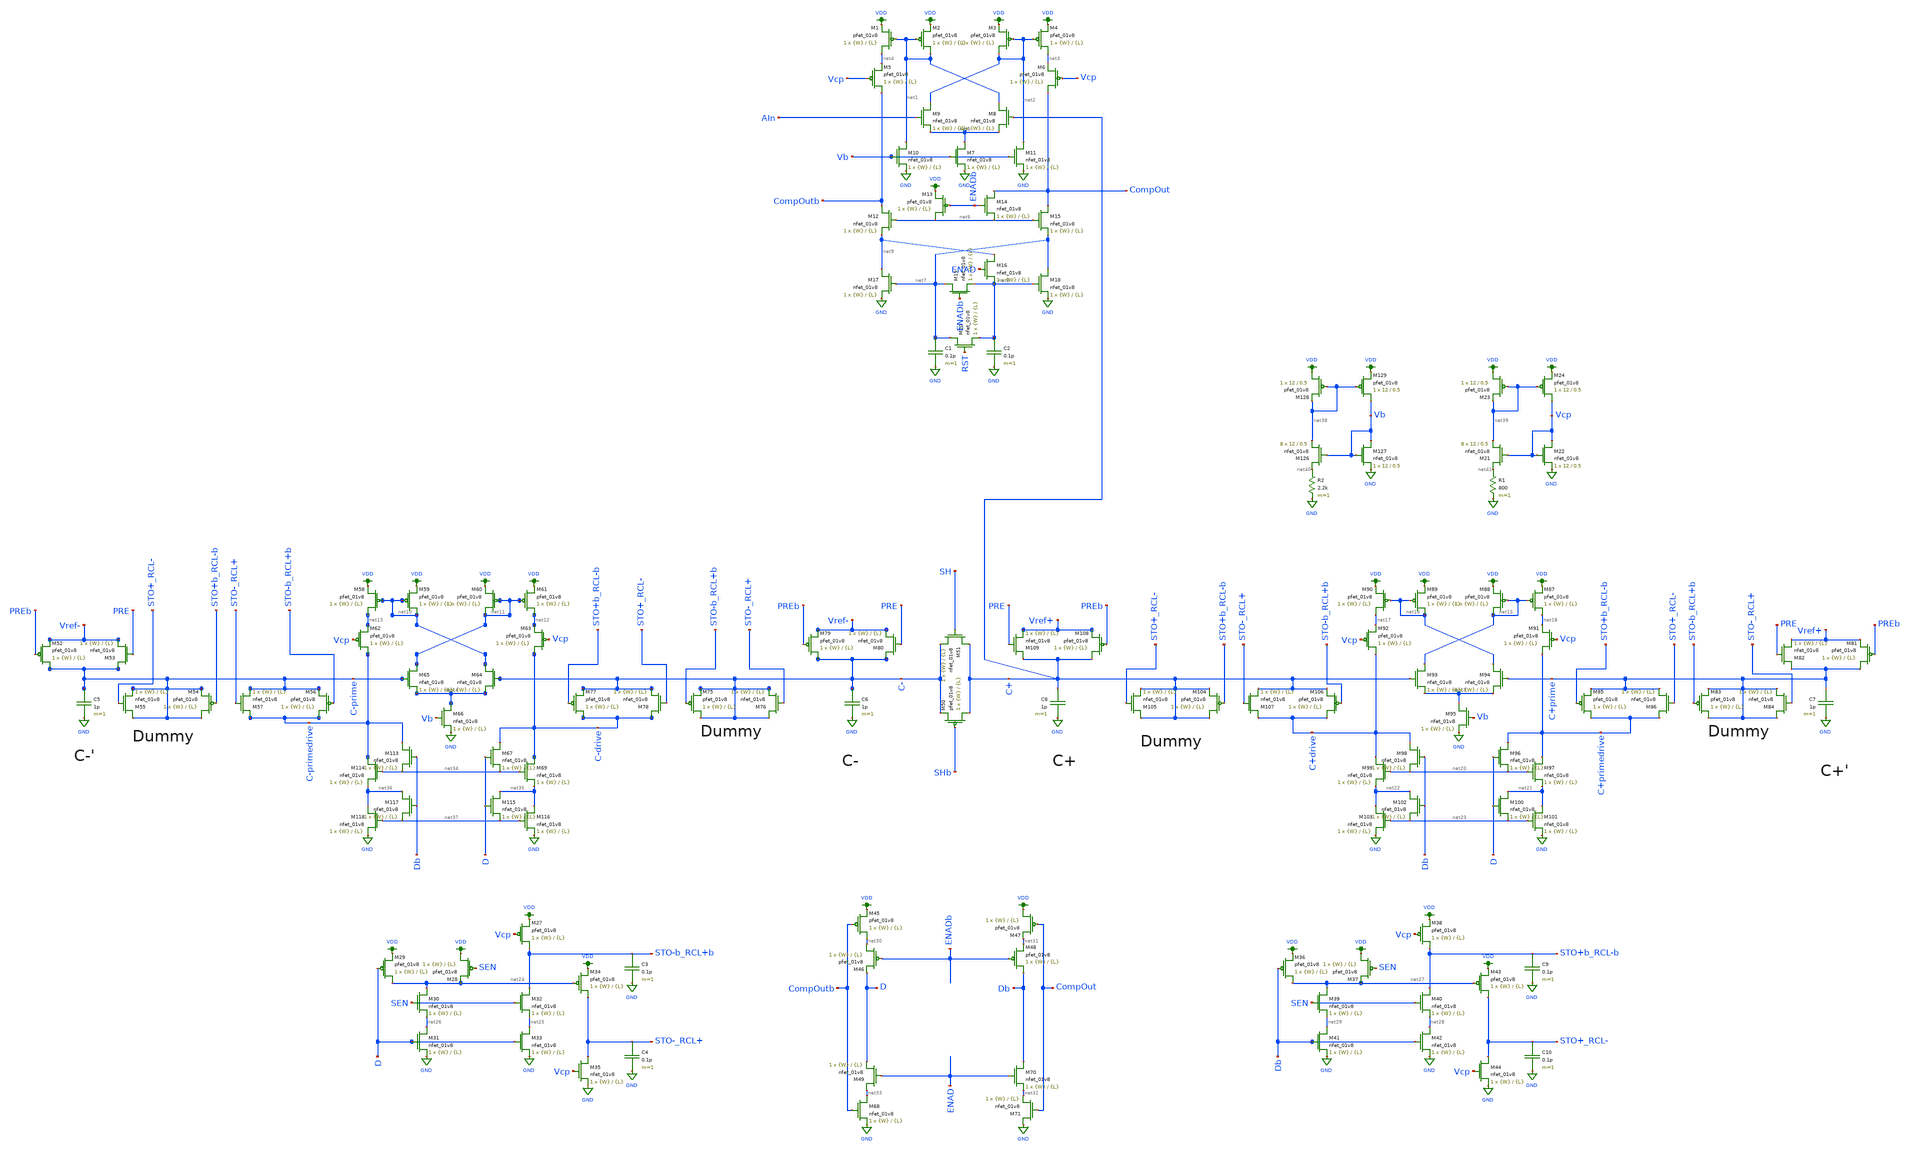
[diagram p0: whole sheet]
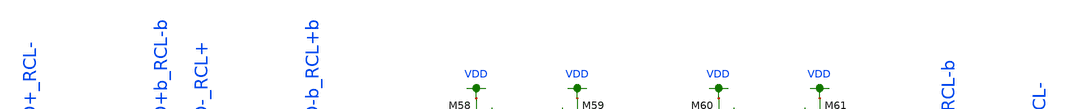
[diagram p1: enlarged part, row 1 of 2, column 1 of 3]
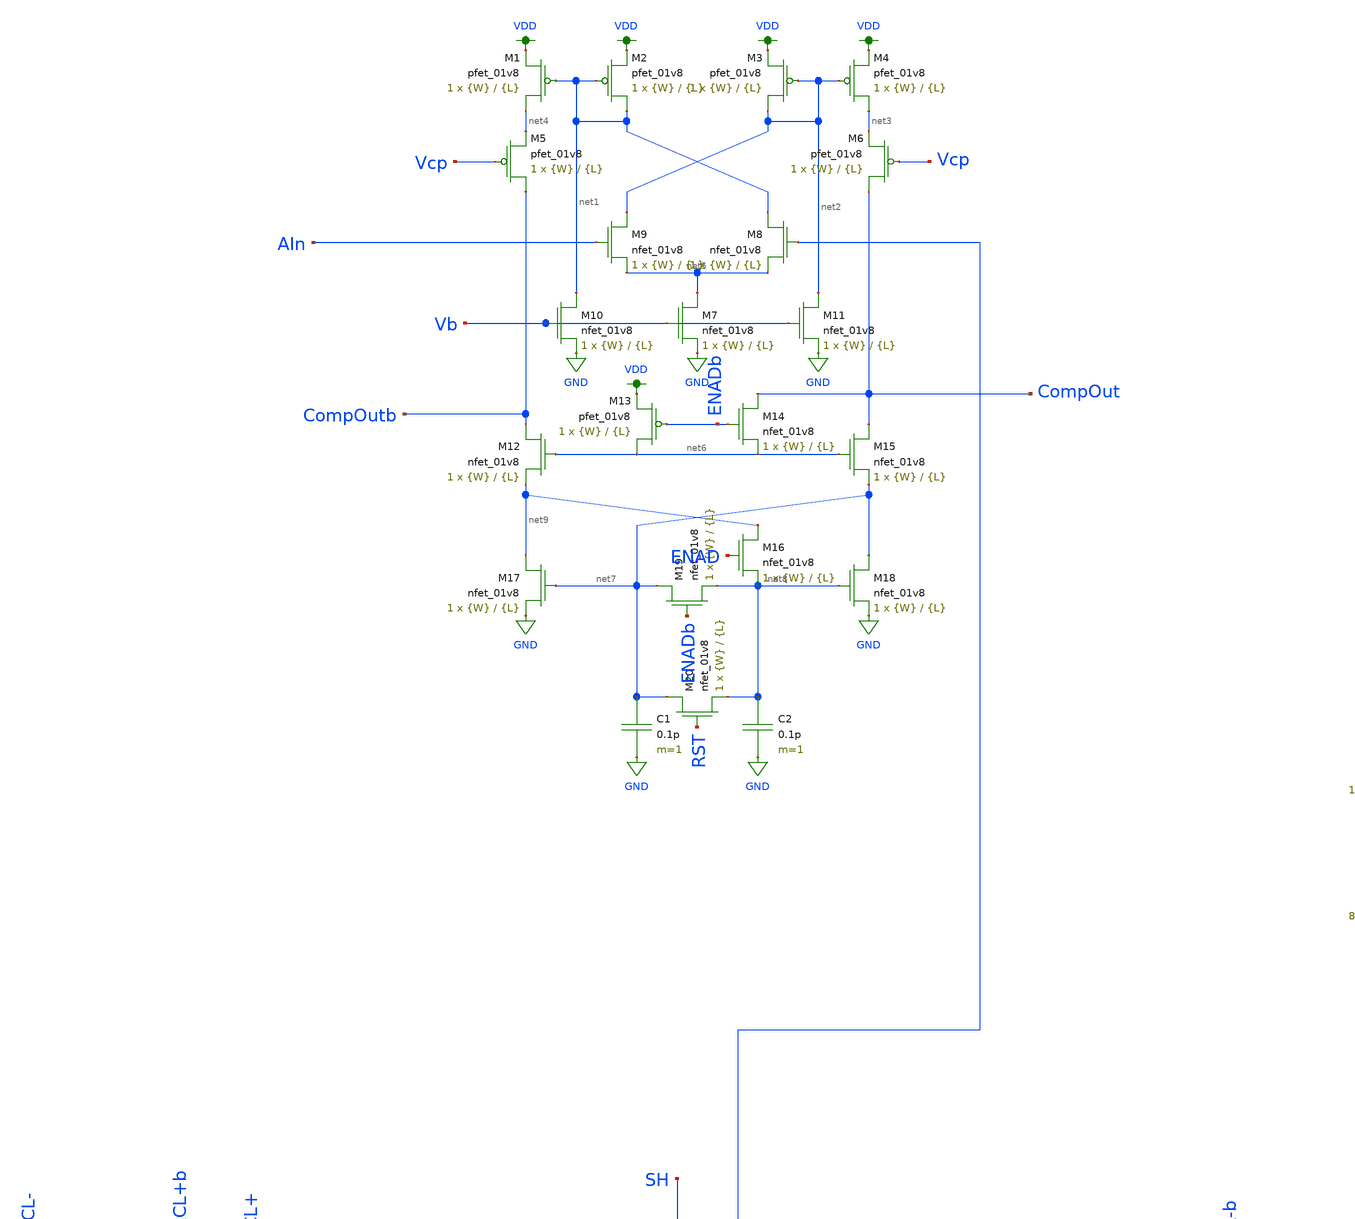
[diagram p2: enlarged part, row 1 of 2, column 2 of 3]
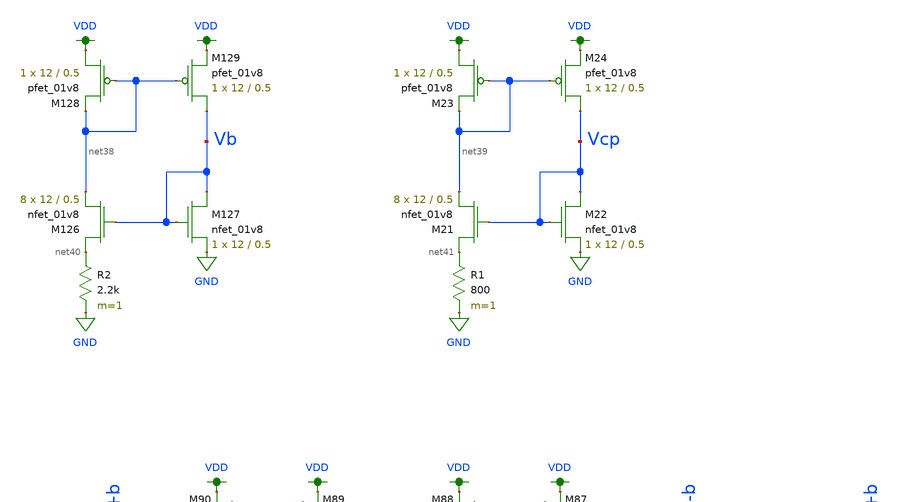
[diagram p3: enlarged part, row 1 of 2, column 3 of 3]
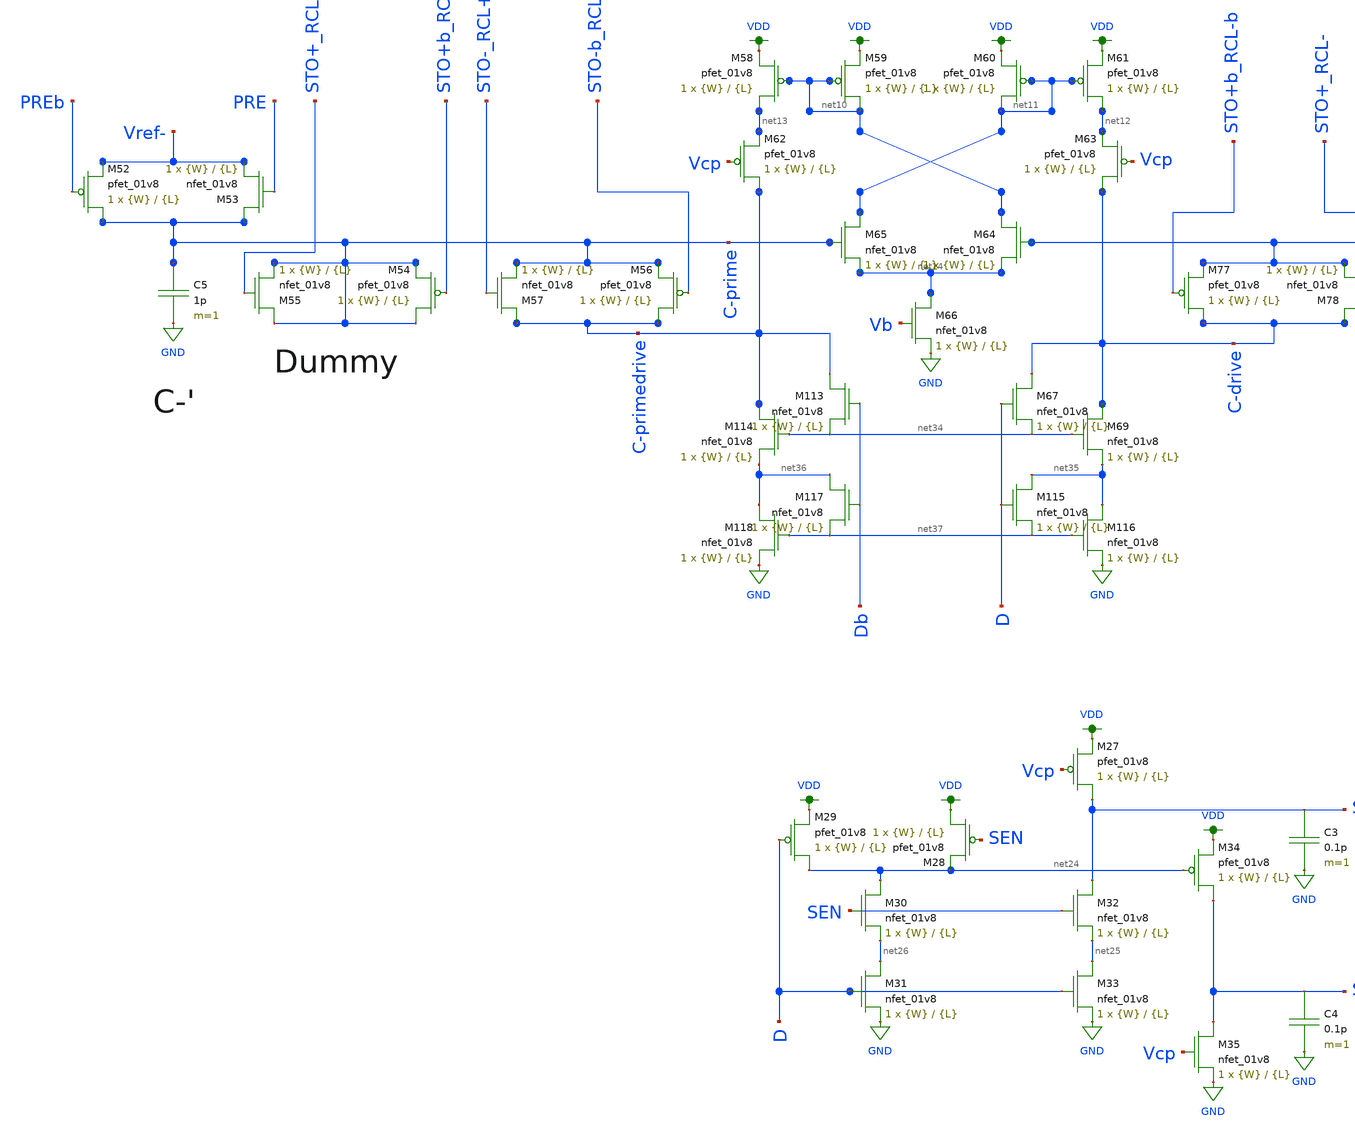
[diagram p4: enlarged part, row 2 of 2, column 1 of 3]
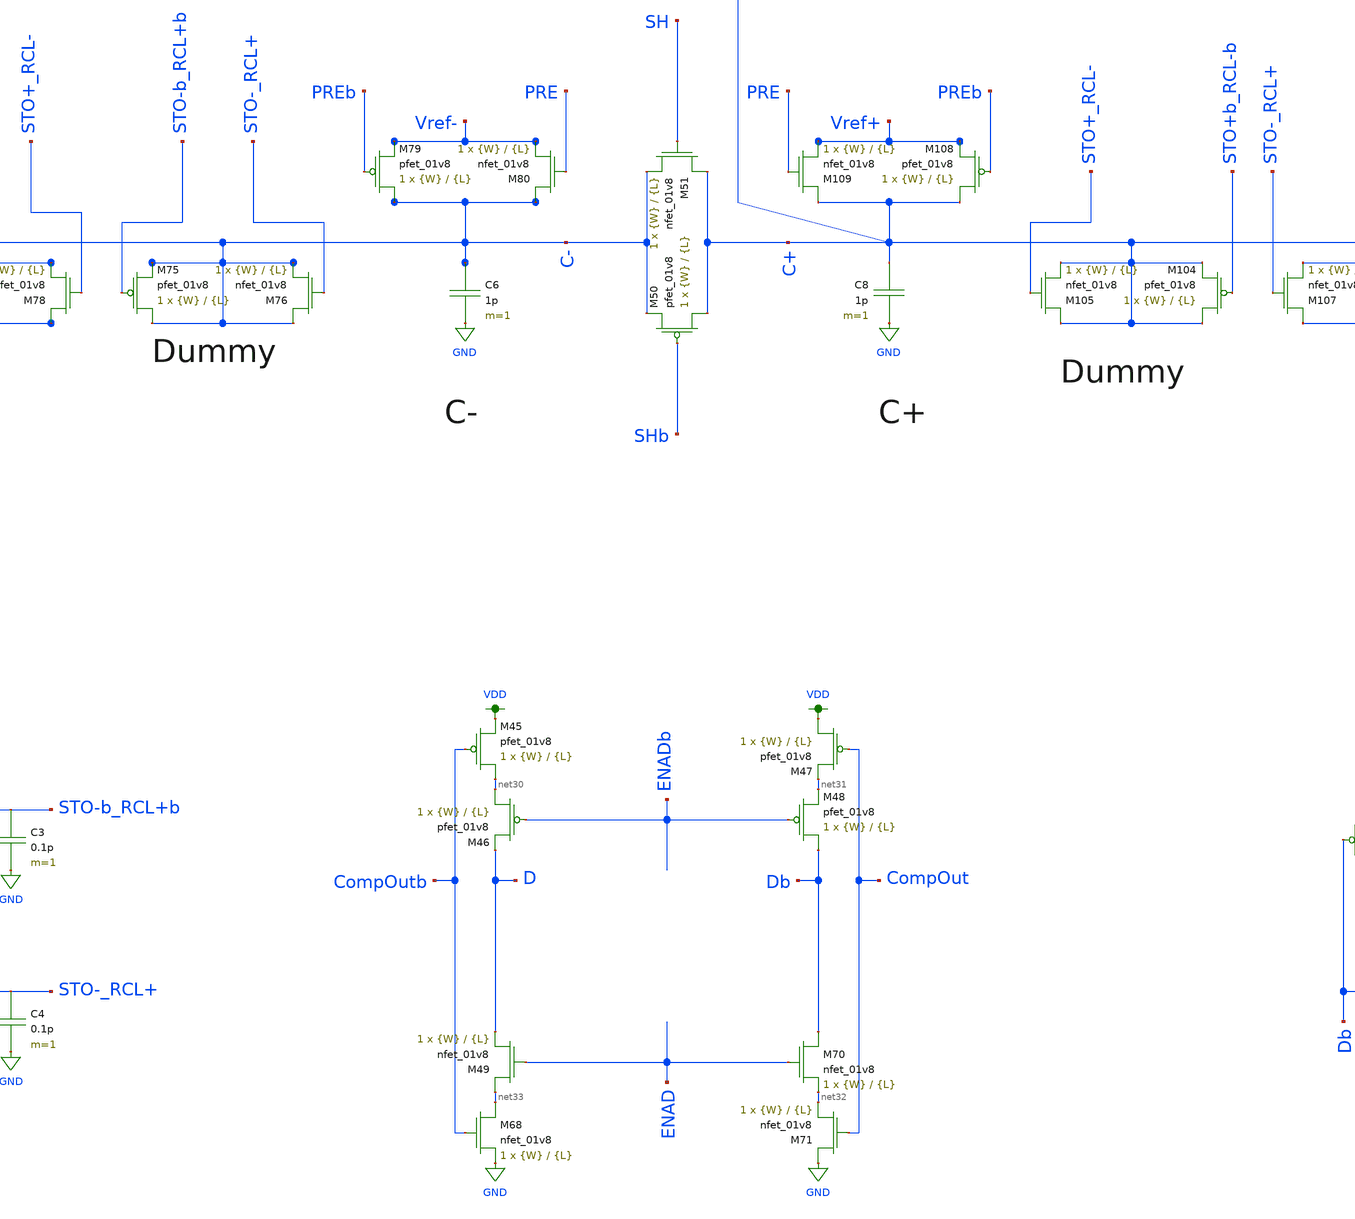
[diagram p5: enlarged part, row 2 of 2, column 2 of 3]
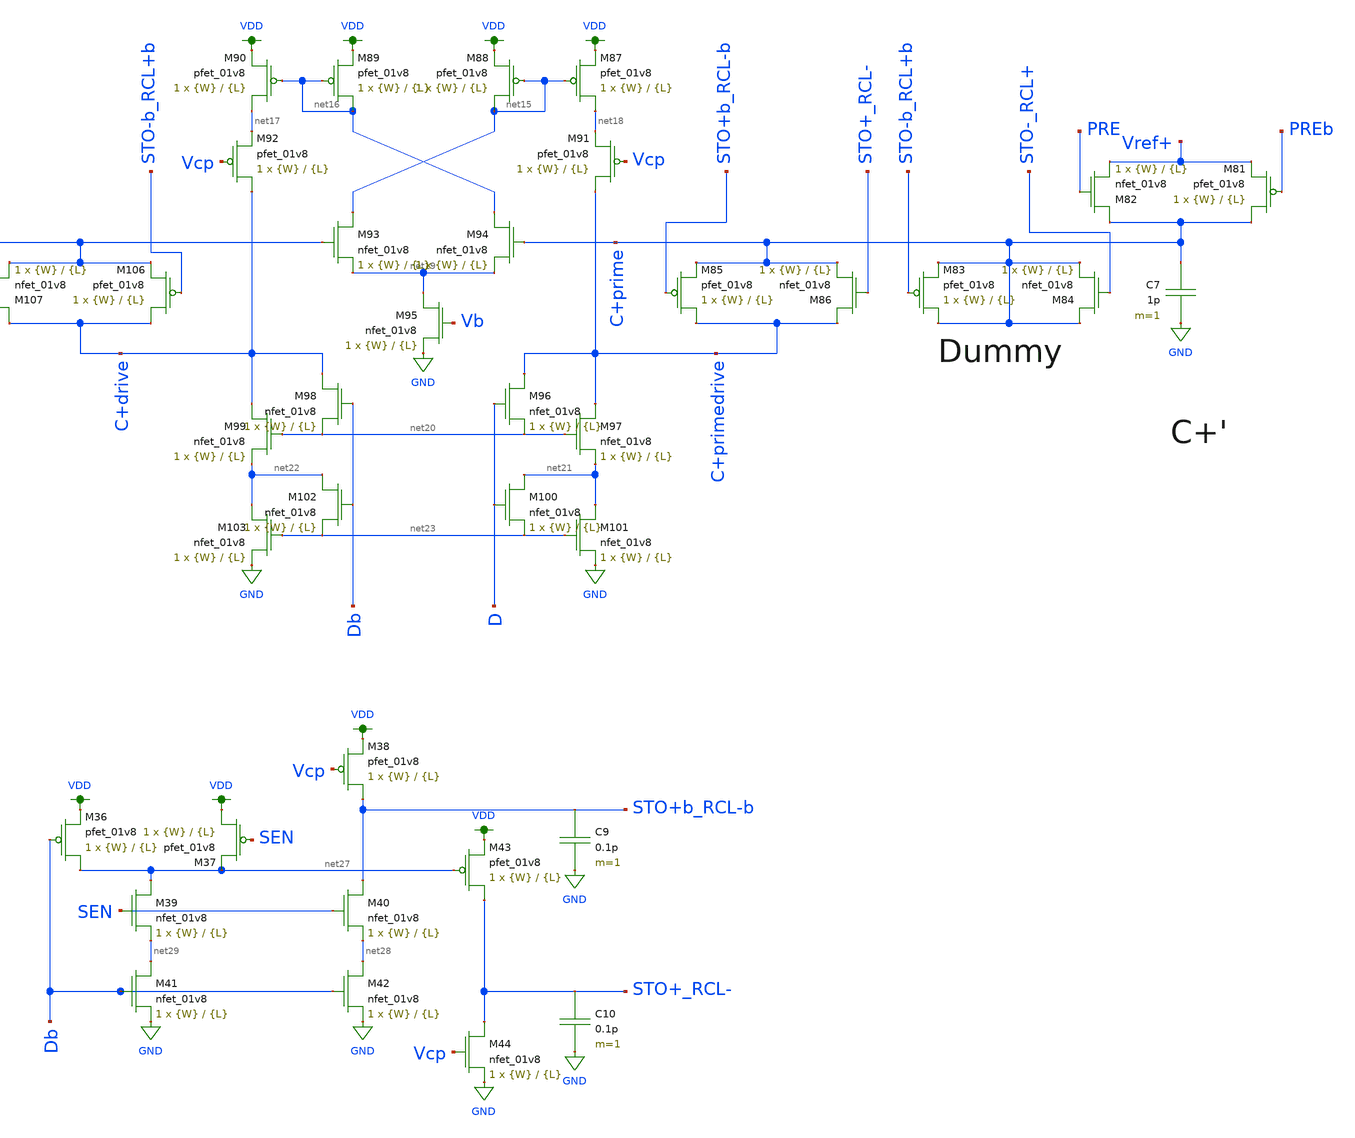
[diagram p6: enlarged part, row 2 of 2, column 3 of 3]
** sch_path: schematics/LDS/all_schematics.sch
**.subckt all_schematics
XM1 net4 net1 VDD VDD sky130_fd_pr__pfet_01v8 L={L} W={W} nf=1 ad='int((nf+1)/2) * W/nf * 0.29' as='int((nf+2)/2) * W/nf * 0.29'
+ pd='2*int((nf+1)/2) * (W/nf + 0.29)' ps='2*int((nf+2)/2) * (W/nf + 0.29)' nrd='0.29 / W' nrs='0.29 / W'
+ sa=0 sb=0 sd=0 mult=1 m=1
XM2 net1 net1 VDD VDD sky130_fd_pr__pfet_01v8 L={L} W={W} nf=1 ad='int((nf+1)/2) * W/nf * 0.29' as='int((nf+2)/2) * W/nf * 0.29'
+ pd='2*int((nf+1)/2) * (W/nf + 0.29)' ps='2*int((nf+2)/2) * (W/nf + 0.29)' nrd='0.29 / W' nrs='0.29 / W'
+ sa=0 sb=0 sd=0 mult=1 m=1
XM3 net2 net2 VDD VDD sky130_fd_pr__pfet_01v8 L={L} W={W} nf=1 ad='int((nf+1)/2) * W/nf * 0.29' as='int((nf+2)/2) * W/nf * 0.29'
+ pd='2*int((nf+1)/2) * (W/nf + 0.29)' ps='2*int((nf+2)/2) * (W/nf + 0.29)' nrd='0.29 / W' nrs='0.29 / W'
+ sa=0 sb=0 sd=0 mult=1 m=1
XM4 net3 net2 VDD VDD sky130_fd_pr__pfet_01v8 L={L} W={W} nf=1 ad='int((nf+1)/2) * W/nf * 0.29' as='int((nf+2)/2) * W/nf * 0.29'
+ pd='2*int((nf+1)/2) * (W/nf + 0.29)' ps='2*int((nf+2)/2) * (W/nf + 0.29)' nrd='0.29 / W' nrs='0.29 / W'
+ sa=0 sb=0 sd=0 mult=1 m=1
XM5 CompOutb Vcp net4 VDD sky130_fd_pr__pfet_01v8 L={L} W={W} nf=1 ad='int((nf+1)/2) * W/nf * 0.29' as='int((nf+2)/2) * W/nf * 0.29'
+ pd='2*int((nf+1)/2) * (W/nf + 0.29)' ps='2*int((nf+2)/2) * (W/nf + 0.29)' nrd='0.29 / W' nrs='0.29 / W'
+ sa=0 sb=0 sd=0 mult=1 m=1
XM6 CompOut Vcp net3 VDD sky130_fd_pr__pfet_01v8 L={L} W={W} nf=1 ad='int((nf+1)/2) * W/nf * 0.29' as='int((nf+2)/2) * W/nf * 0.29'
+ pd='2*int((nf+1)/2) * (W/nf + 0.29)' ps='2*int((nf+2)/2) * (W/nf + 0.29)' nrd='0.29 / W' nrs='0.29 / W'
+ sa=0 sb=0 sd=0 mult=1 m=1
XM7 net5 Vb GND GND sky130_fd_pr__nfet_01v8 L={L} W={W} nf=1 ad='int((nf+1)/2) * W/nf * 0.29' as='int((nf+2)/2) * W/nf * 0.29'
+ pd='2*int((nf+1)/2) * (W/nf + 0.29)' ps='2*int((nf+2)/2) * (W/nf + 0.29)' nrd='0.29 / W' nrs='0.29 / W'
+ sa=0 sb=0 sd=0 mult=1 m=1
XM8 net1 C+ net5 GND sky130_fd_pr__nfet_01v8 L={L} W={W} nf=1 ad='int((nf+1)/2) * W/nf * 0.29' as='int((nf+2)/2) * W/nf * 0.29'
+ pd='2*int((nf+1)/2) * (W/nf + 0.29)' ps='2*int((nf+2)/2) * (W/nf + 0.29)' nrd='0.29 / W' nrs='0.29 / W'
+ sa=0 sb=0 sd=0 mult=1 m=1
XM9 net2 AIn net5 GND sky130_fd_pr__nfet_01v8 L={L} W={W} nf=1 ad='int((nf+1)/2) * W/nf * 0.29' as='int((nf+2)/2) * W/nf * 0.29'
+ pd='2*int((nf+1)/2) * (W/nf + 0.29)' ps='2*int((nf+2)/2) * (W/nf + 0.29)' nrd='0.29 / W' nrs='0.29 / W'
+ sa=0 sb=0 sd=0 mult=1 m=1
XM10 net1 Vb GND GND sky130_fd_pr__nfet_01v8 L={L} W={W} nf=1 ad='int((nf+1)/2) * W/nf * 0.29' as='int((nf+2)/2) * W/nf * 0.29'
+ pd='2*int((nf+1)/2) * (W/nf + 0.29)' ps='2*int((nf+2)/2) * (W/nf + 0.29)' nrd='0.29 / W' nrs='0.29 / W'
+ sa=0 sb=0 sd=0 mult=1 m=1
XM11 net2 Vb GND GND sky130_fd_pr__nfet_01v8 L={L} W={W} nf=1 ad='int((nf+1)/2) * W/nf * 0.29' as='int((nf+2)/2) * W/nf * 0.29'
+ pd='2*int((nf+1)/2) * (W/nf + 0.29)' ps='2*int((nf+2)/2) * (W/nf + 0.29)' nrd='0.29 / W' nrs='0.29 / W'
+ sa=0 sb=0 sd=0 mult=1 m=1
XM12 CompOutb net6 net9 GND sky130_fd_pr__nfet_01v8 L={L} W={W} nf=1 ad='int((nf+1)/2) * W/nf * 0.29'
+ as='int((nf+2)/2) * W/nf * 0.29' pd='2*int((nf+1)/2) * (W/nf + 0.29)' ps='2*int((nf+2)/2) * (W/nf + 0.29)'
+ nrd='0.29 / W' nrs='0.29 / W' sa=0 sb=0 sd=0 mult=1 m=1
XM13 net6 ENADb VDD VDD sky130_fd_pr__pfet_01v8 L={L} W={W} nf=1 ad='int((nf+1)/2) * W/nf * 0.29' as='int((nf+2)/2) * W/nf * 0.29'
+ pd='2*int((nf+1)/2) * (W/nf + 0.29)' ps='2*int((nf+2)/2) * (W/nf + 0.29)' nrd='0.29 / W' nrs='0.29 / W'
+ sa=0 sb=0 sd=0 mult=1 m=1
XM14 CompOut ENADb net6 GND sky130_fd_pr__nfet_01v8 L={L} W={W} nf=1 ad='int((nf+1)/2) * W/nf * 0.29'
+ as='int((nf+2)/2) * W/nf * 0.29' pd='2*int((nf+1)/2) * (W/nf + 0.29)' ps='2*int((nf+2)/2) * (W/nf + 0.29)'
+ nrd='0.29 / W' nrs='0.29 / W' sa=0 sb=0 sd=0 mult=1 m=1
XM15 CompOut net6 net7 GND sky130_fd_pr__nfet_01v8 L={L} W={W} nf=1 ad='int((nf+1)/2) * W/nf * 0.29'
+ as='int((nf+2)/2) * W/nf * 0.29' pd='2*int((nf+1)/2) * (W/nf + 0.29)' ps='2*int((nf+2)/2) * (W/nf + 0.29)'
+ nrd='0.29 / W' nrs='0.29 / W' sa=0 sb=0 sd=0 mult=1 m=1
XM16 net9 ENAD net8 GND sky130_fd_pr__nfet_01v8 L={L} W={W} nf=1 ad='int((nf+1)/2) * W/nf * 0.29' as='int((nf+2)/2) * W/nf * 0.29'
+ pd='2*int((nf+1)/2) * (W/nf + 0.29)' ps='2*int((nf+2)/2) * (W/nf + 0.29)' nrd='0.29 / W' nrs='0.29 / W'
+ sa=0 sb=0 sd=0 mult=1 m=1
XM17 net9 net7 GND GND sky130_fd_pr__nfet_01v8 L={L} W={W} nf=1 ad='int((nf+1)/2) * W/nf * 0.29' as='int((nf+2)/2) * W/nf * 0.29'
+ pd='2*int((nf+1)/2) * (W/nf + 0.29)' ps='2*int((nf+2)/2) * (W/nf + 0.29)' nrd='0.29 / W' nrs='0.29 / W'
+ sa=0 sb=0 sd=0 mult=1 m=1
XM18 net7 net8 GND GND sky130_fd_pr__nfet_01v8 L={L} W={W} nf=1 ad='int((nf+1)/2) * W/nf * 0.29' as='int((nf+2)/2) * W/nf * 0.29'
+ pd='2*int((nf+1)/2) * (W/nf + 0.29)' ps='2*int((nf+2)/2) * (W/nf + 0.29)' nrd='0.29 / W' nrs='0.29 / W'
+ sa=0 sb=0 sd=0 mult=1 m=1
XM19 net7 ENADb net8 GND sky130_fd_pr__nfet_01v8 L={L} W={W} nf=1 ad='int((nf+1)/2) * W/nf * 0.29' as='int((nf+2)/2) * W/nf * 0.29'
+ pd='2*int((nf+1)/2) * (W/nf + 0.29)' ps='2*int((nf+2)/2) * (W/nf + 0.29)' nrd='0.29 / W' nrs='0.29 / W'
+ sa=0 sb=0 sd=0 mult=1 m=1
XM20 net7 RST net8 GND sky130_fd_pr__nfet_01v8 L={L} W={W} nf=1 ad='int((nf+1)/2) * W/nf * 0.29' as='int((nf+2)/2) * W/nf * 0.29'
+ pd='2*int((nf+1)/2) * (W/nf + 0.29)' ps='2*int((nf+2)/2) * (W/nf + 0.29)' nrd='0.29 / W' nrs='0.29 / W'
+ sa=0 sb=0 sd=0 mult=1 m=1
C1 net7 GND 0.1p m=1
C2 net8 GND 0.1p m=1
XM50 C+ SHb C- VDD sky130_fd_pr__pfet_01v8 L={L} W={W} nf=1 ad='int((nf+1)/2) * W/nf * 0.29' as='int((nf+2)/2) * W/nf * 0.29'
+ pd='2*int((nf+1)/2) * (W/nf + 0.29)' ps='2*int((nf+2)/2) * (W/nf + 0.29)' nrd='0.29 / W' nrs='0.29 / W'
+ sa=0 sb=0 sd=0 mult=1 m=1
XM51 C+ SH C- GND sky130_fd_pr__nfet_01v8 L={L} W={W} nf=1 ad='int((nf+1)/2) * W/nf * 0.29' as='int((nf+2)/2) * W/nf * 0.29'
+ pd='2*int((nf+1)/2) * (W/nf + 0.29)' ps='2*int((nf+2)/2) * (W/nf + 0.29)' nrd='0.29 / W' nrs='0.29 / W'
+ sa=0 sb=0 sd=0 mult=1 m=1
XM52 C-prime PREb Vref- VDD sky130_fd_pr__pfet_01v8 L={L} W={W} nf=1 ad='int((nf+1)/2) * W/nf * 0.29'
+ as='int((nf+2)/2) * W/nf * 0.29' pd='2*int((nf+1)/2) * (W/nf + 0.29)' ps='2*int((nf+2)/2) * (W/nf + 0.29)'
+ nrd='0.29 / W' nrs='0.29 / W' sa=0 sb=0 sd=0 mult=1 m=1
XM53 C-prime PRE Vref- GND sky130_fd_pr__nfet_01v8 L={L} W={W} nf=1 ad='int((nf+1)/2) * W/nf * 0.29'
+ as='int((nf+2)/2) * W/nf * 0.29' pd='2*int((nf+1)/2) * (W/nf + 0.29)' ps='2*int((nf+2)/2) * (W/nf + 0.29)'
+ nrd='0.29 / W' nrs='0.29 / W' sa=0 sb=0 sd=0 mult=1 m=1
C5 C-prime GND 1p m=1
XM54 C-prime STO+b_RCL-b C-prime VDD sky130_fd_pr__pfet_01v8 L={L} W={W} nf=1 ad='int((nf+1)/2) * W/nf * 0.29'
+ as='int((nf+2)/2) * W/nf * 0.29' pd='2*int((nf+1)/2) * (W/nf + 0.29)' ps='2*int((nf+2)/2) * (W/nf + 0.29)'
+ nrd='0.29 / W' nrs='0.29 / W' sa=0 sb=0 sd=0 mult=1 m=1
XM55 C-prime STO+_RCL- C-prime GND sky130_fd_pr__nfet_01v8 L={L} W={W} nf=1 ad='int((nf+1)/2) * W/nf * 0.29'
+ as='int((nf+2)/2) * W/nf * 0.29' pd='2*int((nf+1)/2) * (W/nf + 0.29)' ps='2*int((nf+2)/2) * (W/nf + 0.29)'
+ nrd='0.29 / W' nrs='0.29 / W' sa=0 sb=0 sd=0 mult=1 m=1
XM56 C-primedrive STO-b_RCL+b C-prime VDD sky130_fd_pr__pfet_01v8 L={L} W={W} nf=1 ad='int((nf+1)/2) * W/nf * 0.29'
+ as='int((nf+2)/2) * W/nf * 0.29' pd='2*int((nf+1)/2) * (W/nf + 0.29)' ps='2*int((nf+2)/2) * (W/nf + 0.29)'
+ nrd='0.29 / W' nrs='0.29 / W' sa=0 sb=0 sd=0 mult=1 m=1
XM57 C-primedrive STO-_RCL+ C-prime GND sky130_fd_pr__nfet_01v8 L={L} W={W} nf=1 ad='int((nf+1)/2) * W/nf * 0.29'
+ as='int((nf+2)/2) * W/nf * 0.29' pd='2*int((nf+1)/2) * (W/nf + 0.29)' ps='2*int((nf+2)/2) * (W/nf + 0.29)'
+ nrd='0.29 / W' nrs='0.29 / W' sa=0 sb=0 sd=0 mult=1 m=1
XM58 net13 net10 VDD VDD sky130_fd_pr__pfet_01v8 L={L} W={W} nf=1 ad='int((nf+1)/2) * W/nf * 0.29' as='int((nf+2)/2) * W/nf * 0.29'
+ pd='2*int((nf+1)/2) * (W/nf + 0.29)' ps='2*int((nf+2)/2) * (W/nf + 0.29)' nrd='0.29 / W' nrs='0.29 / W'
+ sa=0 sb=0 sd=0 mult=1 m=1
XM59 net10 net10 VDD VDD sky130_fd_pr__pfet_01v8 L={L} W={W} nf=1 ad='int((nf+1)/2) * W/nf * 0.29' as='int((nf+2)/2) * W/nf * 0.29'
+ pd='2*int((nf+1)/2) * (W/nf + 0.29)' ps='2*int((nf+2)/2) * (W/nf + 0.29)' nrd='0.29 / W' nrs='0.29 / W'
+ sa=0 sb=0 sd=0 mult=1 m=1
XM60 net11 net11 VDD VDD sky130_fd_pr__pfet_01v8 L={L} W={W} nf=1 ad='int((nf+1)/2) * W/nf * 0.29' as='int((nf+2)/2) * W/nf * 0.29'
+ pd='2*int((nf+1)/2) * (W/nf + 0.29)' ps='2*int((nf+2)/2) * (W/nf + 0.29)' nrd='0.29 / W' nrs='0.29 / W'
+ sa=0 sb=0 sd=0 mult=1 m=1
XM61 net12 net11 VDD VDD sky130_fd_pr__pfet_01v8 L={L} W={W} nf=1 ad='int((nf+1)/2) * W/nf * 0.29' as='int((nf+2)/2) * W/nf * 0.29'
+ pd='2*int((nf+1)/2) * (W/nf + 0.29)' ps='2*int((nf+2)/2) * (W/nf + 0.29)' nrd='0.29 / W' nrs='0.29 / W'
+ sa=0 sb=0 sd=0 mult=1 m=1
XM62 C-primedrive Vcp net13 VDD sky130_fd_pr__pfet_01v8 L={L} W={W} nf=1 ad='int((nf+1)/2) * W/nf * 0.29'
+ as='int((nf+2)/2) * W/nf * 0.29' pd='2*int((nf+1)/2) * (W/nf + 0.29)' ps='2*int((nf+2)/2) * (W/nf + 0.29)'
+ nrd='0.29 / W' nrs='0.29 / W' sa=0 sb=0 sd=0 mult=1 m=1
XM63 C-drive Vcp net12 VDD sky130_fd_pr__pfet_01v8 L={L} W={W} nf=1 ad='int((nf+1)/2) * W/nf * 0.29'
+ as='int((nf+2)/2) * W/nf * 0.29' pd='2*int((nf+1)/2) * (W/nf + 0.29)' ps='2*int((nf+2)/2) * (W/nf + 0.29)'
+ nrd='0.29 / W' nrs='0.29 / W' sa=0 sb=0 sd=0 mult=1 m=1
XM64 net10 C- net14 GND sky130_fd_pr__nfet_01v8 L={L} W={W} nf=1 ad='int((nf+1)/2) * W/nf * 0.29' as='int((nf+2)/2) * W/nf * 0.29'
+ pd='2*int((nf+1)/2) * (W/nf + 0.29)' ps='2*int((nf+2)/2) * (W/nf + 0.29)' nrd='0.29 / W' nrs='0.29 / W'
+ sa=0 sb=0 sd=0 mult=1 m=1
XM65 net11 C-prime net14 GND sky130_fd_pr__nfet_01v8 L={L} W={W} nf=1 ad='int((nf+1)/2) * W/nf * 0.29'
+ as='int((nf+2)/2) * W/nf * 0.29' pd='2*int((nf+1)/2) * (W/nf + 0.29)' ps='2*int((nf+2)/2) * (W/nf + 0.29)'
+ nrd='0.29 / W' nrs='0.29 / W' sa=0 sb=0 sd=0 mult=1 m=1
XM66 net14 Vb GND GND sky130_fd_pr__nfet_01v8 L={L} W={W} nf=1 ad='int((nf+1)/2) * W/nf * 0.29' as='int((nf+2)/2) * W/nf * 0.29'
+ pd='2*int((nf+1)/2) * (W/nf + 0.29)' ps='2*int((nf+2)/2) * (W/nf + 0.29)' nrd='0.29 / W' nrs='0.29 / W'
+ sa=0 sb=0 sd=0 mult=1 m=1
XM75 C- STO-b_RCL+b C- VDD sky130_fd_pr__pfet_01v8 L={L} W={W} nf=1 ad='int((nf+1)/2) * W/nf * 0.29'
+ as='int((nf+2)/2) * W/nf * 0.29' pd='2*int((nf+1)/2) * (W/nf + 0.29)' ps='2*int((nf+2)/2) * (W/nf + 0.29)'
+ nrd='0.29 / W' nrs='0.29 / W' sa=0 sb=0 sd=0 mult=1 m=1
XM76 C- STO-_RCL+ C- GND sky130_fd_pr__nfet_01v8 L={L} W={W} nf=1 ad='int((nf+1)/2) * W/nf * 0.29' as='int((nf+2)/2) * W/nf * 0.29'
+ pd='2*int((nf+1)/2) * (W/nf + 0.29)' ps='2*int((nf+2)/2) * (W/nf + 0.29)' nrd='0.29 / W' nrs='0.29 / W'
+ sa=0 sb=0 sd=0 mult=1 m=1
XM77 C-drive STO+b_RCL-b C- VDD sky130_fd_pr__pfet_01v8 L={L} W={W} nf=1 ad='int((nf+1)/2) * W/nf * 0.29'
+ as='int((nf+2)/2) * W/nf * 0.29' pd='2*int((nf+1)/2) * (W/nf + 0.29)' ps='2*int((nf+2)/2) * (W/nf + 0.29)'
+ nrd='0.29 / W' nrs='0.29 / W' sa=0 sb=0 sd=0 mult=1 m=1
XM78 C-drive STO+_RCL- C- GND sky130_fd_pr__nfet_01v8 L={L} W={W} nf=1 ad='int((nf+1)/2) * W/nf * 0.29'
+ as='int((nf+2)/2) * W/nf * 0.29' pd='2*int((nf+1)/2) * (W/nf + 0.29)' ps='2*int((nf+2)/2) * (W/nf + 0.29)'
+ nrd='0.29 / W' nrs='0.29 / W' sa=0 sb=0 sd=0 mult=1 m=1
XM79 C- PREb Vref- VDD sky130_fd_pr__pfet_01v8 L={L} W={W} nf=1 ad='int((nf+1)/2) * W/nf * 0.29' as='int((nf+2)/2) * W/nf * 0.29'
+ pd='2*int((nf+1)/2) * (W/nf + 0.29)' ps='2*int((nf+2)/2) * (W/nf + 0.29)' nrd='0.29 / W' nrs='0.29 / W'
+ sa=0 sb=0 sd=0 mult=1 m=1
XM80 C- PRE Vref- GND sky130_fd_pr__nfet_01v8 L={L} W={W} nf=1 ad='int((nf+1)/2) * W/nf * 0.29' as='int((nf+2)/2) * W/nf * 0.29'
+ pd='2*int((nf+1)/2) * (W/nf + 0.29)' ps='2*int((nf+2)/2) * (W/nf + 0.29)' nrd='0.29 / W' nrs='0.29 / W'
+ sa=0 sb=0 sd=0 mult=1 m=1
C6 C- GND 1p m=1
XM81 C+prime PREb Vref+ VDD sky130_fd_pr__pfet_01v8 L={L} W={W} nf=1 ad='int((nf+1)/2) * W/nf * 0.29'
+ as='int((nf+2)/2) * W/nf * 0.29' pd='2*int((nf+1)/2) * (W/nf + 0.29)' ps='2*int((nf+2)/2) * (W/nf + 0.29)'
+ nrd='0.29 / W' nrs='0.29 / W' sa=0 sb=0 sd=0 mult=1 m=1
XM82 C+prime PRE Vref+ GND sky130_fd_pr__nfet_01v8 L={L} W={W} nf=1 ad='int((nf+1)/2) * W/nf * 0.29'
+ as='int((nf+2)/2) * W/nf * 0.29' pd='2*int((nf+1)/2) * (W/nf + 0.29)' ps='2*int((nf+2)/2) * (W/nf + 0.29)'
+ nrd='0.29 / W' nrs='0.29 / W' sa=0 sb=0 sd=0 mult=1 m=1
C7 C+prime GND 1p m=1
XM83 C+prime STO-b_RCL+b C+prime VDD sky130_fd_pr__pfet_01v8 L={L} W={W} nf=1 ad='int((nf+1)/2) * W/nf * 0.29'
+ as='int((nf+2)/2) * W/nf * 0.29' pd='2*int((nf+1)/2) * (W/nf + 0.29)' ps='2*int((nf+2)/2) * (W/nf + 0.29)'
+ nrd='0.29 / W' nrs='0.29 / W' sa=0 sb=0 sd=0 mult=1 m=1
XM84 C+prime STO-_RCL+ C+prime GND sky130_fd_pr__nfet_01v8 L={L} W={W} nf=1 ad='int((nf+1)/2) * W/nf * 0.29'
+ as='int((nf+2)/2) * W/nf * 0.29' pd='2*int((nf+1)/2) * (W/nf + 0.29)' ps='2*int((nf+2)/2) * (W/nf + 0.29)'
+ nrd='0.29 / W' nrs='0.29 / W' sa=0 sb=0 sd=0 mult=1 m=1
XM85 C+primedrive STO+b_RCL-b C+prime VDD sky130_fd_pr__pfet_01v8 L={L} W={W} nf=1 ad='int((nf+1)/2) * W/nf * 0.29'
+ as='int((nf+2)/2) * W/nf * 0.29' pd='2*int((nf+1)/2) * (W/nf + 0.29)' ps='2*int((nf+2)/2) * (W/nf + 0.29)'
+ nrd='0.29 / W' nrs='0.29 / W' sa=0 sb=0 sd=0 mult=1 m=1
XM86 C+primedrive STO+_RCL- C+prime GND sky130_fd_pr__nfet_01v8 L={L} W={W} nf=1 ad='int((nf+1)/2) * W/nf * 0.29'
+ as='int((nf+2)/2) * W/nf * 0.29' pd='2*int((nf+1)/2) * (W/nf + 0.29)' ps='2*int((nf+2)/2) * (W/nf + 0.29)'
+ nrd='0.29 / W' nrs='0.29 / W' sa=0 sb=0 sd=0 mult=1 m=1
XM87 net18 net15 VDD VDD sky130_fd_pr__pfet_01v8 L={L} W={W} nf=1 ad='int((nf+1)/2) * W/nf * 0.29' as='int((nf+2)/2) * W/nf * 0.29'
+ pd='2*int((nf+1)/2) * (W/nf + 0.29)' ps='2*int((nf+2)/2) * (W/nf + 0.29)' nrd='0.29 / W' nrs='0.29 / W'
+ sa=0 sb=0 sd=0 mult=1 m=1
XM88 net15 net15 VDD VDD sky130_fd_pr__pfet_01v8 L={L} W={W} nf=1 ad='int((nf+1)/2) * W/nf * 0.29' as='int((nf+2)/2) * W/nf * 0.29'
+ pd='2*int((nf+1)/2) * (W/nf + 0.29)' ps='2*int((nf+2)/2) * (W/nf + 0.29)' nrd='0.29 / W' nrs='0.29 / W'
+ sa=0 sb=0 sd=0 mult=1 m=1
XM89 net16 net16 VDD VDD sky130_fd_pr__pfet_01v8 L={L} W={W} nf=1 ad='int((nf+1)/2) * W/nf * 0.29' as='int((nf+2)/2) * W/nf * 0.29'
+ pd='2*int((nf+1)/2) * (W/nf + 0.29)' ps='2*int((nf+2)/2) * (W/nf + 0.29)' nrd='0.29 / W' nrs='0.29 / W'
+ sa=0 sb=0 sd=0 mult=1 m=1
XM90 net17 net16 VDD VDD sky130_fd_pr__pfet_01v8 L={L} W={W} nf=1 ad='int((nf+1)/2) * W/nf * 0.29' as='int((nf+2)/2) * W/nf * 0.29'
+ pd='2*int((nf+1)/2) * (W/nf + 0.29)' ps='2*int((nf+2)/2) * (W/nf + 0.29)' nrd='0.29 / W' nrs='0.29 / W'
+ sa=0 sb=0 sd=0 mult=1 m=1
XM91 C+primedrive Vcp net18 VDD sky130_fd_pr__pfet_01v8 L={L} W={W} nf=1 ad='int((nf+1)/2) * W/nf * 0.29'
+ as='int((nf+2)/2) * W/nf * 0.29' pd='2*int((nf+1)/2) * (W/nf + 0.29)' ps='2*int((nf+2)/2) * (W/nf + 0.29)'
+ nrd='0.29 / W' nrs='0.29 / W' sa=0 sb=0 sd=0 mult=1 m=1
XM92 C+drive Vcp net17 VDD sky130_fd_pr__pfet_01v8 L={L} W={W} nf=1 ad='int((nf+1)/2) * W/nf * 0.29'
+ as='int((nf+2)/2) * W/nf * 0.29' pd='2*int((nf+1)/2) * (W/nf + 0.29)' ps='2*int((nf+2)/2) * (W/nf + 0.29)'
+ nrd='0.29 / W' nrs='0.29 / W' sa=0 sb=0 sd=0 mult=1 m=1
XM93 net15 C+ net19 GND sky130_fd_pr__nfet_01v8 L={L} W={W} nf=1 ad='int((nf+1)/2) * W/nf * 0.29' as='int((nf+2)/2) * W/nf * 0.29'
+ pd='2*int((nf+1)/2) * (W/nf + 0.29)' ps='2*int((nf+2)/2) * (W/nf + 0.29)' nrd='0.29 / W' nrs='0.29 / W'
+ sa=0 sb=0 sd=0 mult=1 m=1
XM94 net16 C+prime net19 GND sky130_fd_pr__nfet_01v8 L={L} W={W} nf=1 ad='int((nf+1)/2) * W/nf * 0.29'
+ as='int((nf+2)/2) * W/nf * 0.29' pd='2*int((nf+1)/2) * (W/nf + 0.29)' ps='2*int((nf+2)/2) * (W/nf + 0.29)'
+ nrd='0.29 / W' nrs='0.29 / W' sa=0 sb=0 sd=0 mult=1 m=1
XM95 net19 Vb GND GND sky130_fd_pr__nfet_01v8 L={L} W={W} nf=1 ad='int((nf+1)/2) * W/nf * 0.29' as='int((nf+2)/2) * W/nf * 0.29'
+ pd='2*int((nf+1)/2) * (W/nf + 0.29)' ps='2*int((nf+2)/2) * (W/nf + 0.29)' nrd='0.29 / W' nrs='0.29 / W'
+ sa=0 sb=0 sd=0 mult=1 m=1
XM96 C+primedrive D net20 GND sky130_fd_pr__nfet_01v8 L={L} W={W} nf=1 ad='int((nf+1)/2) * W/nf * 0.29'
+ as='int((nf+2)/2) * W/nf * 0.29' pd='2*int((nf+1)/2) * (W/nf + 0.29)' ps='2*int((nf+2)/2) * (W/nf + 0.29)'
+ nrd='0.29 / W' nrs='0.29 / W' sa=0 sb=0 sd=0 mult=1 m=1
XM97 C+primedrive net20 net21 GND sky130_fd_pr__nfet_01v8 L={L} W={W} nf=1 ad='int((nf+1)/2) * W/nf * 0.29'
+ as='int((nf+2)/2) * W/nf * 0.29' pd='2*int((nf+1)/2) * (W/nf + 0.29)' ps='2*int((nf+2)/2) * (W/nf + 0.29)'
+ nrd='0.29 / W' nrs='0.29 / W' sa=0 sb=0 sd=0 mult=1 m=1
XM98 C+drive Db net20 GND sky130_fd_pr__nfet_01v8 L={L} W={W} nf=1 ad='int((nf+1)/2) * W/nf * 0.29' as='int((nf+2)/2) * W/nf * 0.29'
+ pd='2*int((nf+1)/2) * (W/nf + 0.29)' ps='2*int((nf+2)/2) * (W/nf + 0.29)' nrd='0.29 / W' nrs='0.29 / W'
+ sa=0 sb=0 sd=0 mult=1 m=1
XM99 C+drive net20 net22 GND sky130_fd_pr__nfet_01v8 L={L} W={W} nf=1 ad='int((nf+1)/2) * W/nf * 0.29'
+ as='int((nf+2)/2) * W/nf * 0.29' pd='2*int((nf+1)/2) * (W/nf + 0.29)' ps='2*int((nf+2)/2) * (W/nf + 0.29)'
+ nrd='0.29 / W' nrs='0.29 / W' sa=0 sb=0 sd=0 mult=1 m=1
XM100 net21 D net23 GND sky130_fd_pr__nfet_01v8 L={L} W={W} nf=1 ad='int((nf+1)/2) * W/nf * 0.29' as='int((nf+2)/2) * W/nf * 0.29'
+ pd='2*int((nf+1)/2) * (W/nf + 0.29)' ps='2*int((nf+2)/2) * (W/nf + 0.29)' nrd='0.29 / W' nrs='0.29 / W'
+ sa=0 sb=0 sd=0 mult=1 m=1
XM101 net21 net23 GND GND sky130_fd_pr__nfet_01v8 L={L} W={W} nf=1 ad='int((nf+1)/2) * W/nf * 0.29' as='int((nf+2)/2) * W/nf * 0.29'
+ pd='2*int((nf+1)/2) * (W/nf + 0.29)' ps='2*int((nf+2)/2) * (W/nf + 0.29)' nrd='0.29 / W' nrs='0.29 / W'
+ sa=0 sb=0 sd=0 mult=1 m=1
XM102 net22 Db net23 GND sky130_fd_pr__nfet_01v8 L={L} W={W} nf=1 ad='int((nf+1)/2) * W/nf * 0.29' as='int((nf+2)/2) * W/nf * 0.29'
+ pd='2*int((nf+1)/2) * (W/nf + 0.29)' ps='2*int((nf+2)/2) * (W/nf + 0.29)' nrd='0.29 / W' nrs='0.29 / W'
+ sa=0 sb=0 sd=0 mult=1 m=1
XM103 net22 net23 GND GND sky130_fd_pr__nfet_01v8 L={L} W={W} nf=1 ad='int((nf+1)/2) * W/nf * 0.29' as='int((nf+2)/2) * W/nf * 0.29'
+ pd='2*int((nf+1)/2) * (W/nf + 0.29)' ps='2*int((nf+2)/2) * (W/nf + 0.29)' nrd='0.29 / W' nrs='0.29 / W'
+ sa=0 sb=0 sd=0 mult=1 m=1
XM104 C+ STO+b_RCL-b C+ VDD sky130_fd_pr__pfet_01v8 L={L} W={W} nf=1 ad='int((nf+1)/2) * W/nf * 0.29'
+ as='int((nf+2)/2) * W/nf * 0.29' pd='2*int((nf+1)/2) * (W/nf + 0.29)' ps='2*int((nf+2)/2) * (W/nf + 0.29)'
+ nrd='0.29 / W' nrs='0.29 / W' sa=0 sb=0 sd=0 mult=1 m=1
XM105 C+ STO+_RCL- C+ GND sky130_fd_pr__nfet_01v8 L={L} W={W} nf=1 ad='int((nf+1)/2) * W/nf * 0.29' as='int((nf+2)/2) * W/nf * 0.29'
+ pd='2*int((nf+1)/2) * (W/nf + 0.29)' ps='2*int((nf+2)/2) * (W/nf + 0.29)' nrd='0.29 / W' nrs='0.29 / W'
+ sa=0 sb=0 sd=0 mult=1 m=1
XM106 C+drive STO-b_RCL+b C+ VDD sky130_fd_pr__pfet_01v8 L={L} W={W} nf=1 ad='int((nf+1)/2) * W/nf * 0.29'
+ as='int((nf+2)/2) * W/nf * 0.29' pd='2*int((nf+1)/2) * (W/nf + 0.29)' ps='2*int((nf+2)/2) * (W/nf + 0.29)'
+ nrd='0.29 / W' nrs='0.29 / W' sa=0 sb=0 sd=0 mult=1 m=1
XM107 C+drive STO-_RCL+ C+ GND sky130_fd_pr__nfet_01v8 L={L} W={W} nf=1 ad='int((nf+1)/2) * W/nf * 0.29'
+ as='int((nf+2)/2) * W/nf * 0.29' pd='2*int((nf+1)/2) * (W/nf + 0.29)' ps='2*int((nf+2)/2) * (W/nf + 0.29)'
+ nrd='0.29 / W' nrs='0.29 / W' sa=0 sb=0 sd=0 mult=1 m=1
XM108 C+ PREb Vref+ VDD sky130_fd_pr__pfet_01v8 L={L} W={W} nf=1 ad='int((nf+1)/2) * W/nf * 0.29' as='int((nf+2)/2) * W/nf * 0.29'
+ pd='2*int((nf+1)/2) * (W/nf + 0.29)' ps='2*int((nf+2)/2) * (W/nf + 0.29)' nrd='0.29 / W' nrs='0.29 / W'
+ sa=0 sb=0 sd=0 mult=1 m=1
XM109 C+ PRE Vref+ GND sky130_fd_pr__nfet_01v8 L={L} W={W} nf=1 ad='int((nf+1)/2) * W/nf * 0.29' as='int((nf+2)/2) * W/nf * 0.29'
+ pd='2*int((nf+1)/2) * (W/nf + 0.29)' ps='2*int((nf+2)/2) * (W/nf + 0.29)' nrd='0.29 / W' nrs='0.29 / W'
+ sa=0 sb=0 sd=0 mult=1 m=1
C8 C+ GND 1p m=1
XM29 net24 D VDD VDD sky130_fd_pr__pfet_01v8 L={L} W={W} nf=1 ad='int((nf+1)/2) * W/nf * 0.29' as='int((nf+2)/2) * W/nf * 0.29'
+ pd='2*int((nf+1)/2) * (W/nf + 0.29)' ps='2*int((nf+2)/2) * (W/nf + 0.29)' nrd='0.29 / W' nrs='0.29 / W'
+ sa=0 sb=0 sd=0 mult=1 m=1
XM30 net24 SEN net26 GND sky130_fd_pr__nfet_01v8 L={L} W={W} nf=1 ad='int((nf+1)/2) * W/nf * 0.29' as='int((nf+2)/2) * W/nf * 0.29'
+ pd='2*int((nf+1)/2) * (W/nf + 0.29)' ps='2*int((nf+2)/2) * (W/nf + 0.29)' nrd='0.29 / W' nrs='0.29 / W'
+ sa=0 sb=0 sd=0 mult=1 m=1
C3 STO-b_RCL+b GND 0.1p m=1
C4 STO-_RCL+ GND 0.1p m=1
C9 STO+b_RCL-b GND 0.1p m=1
C10 STO+_RCL- GND 0.1p m=1
XM67 C-drive D net34 GND sky130_fd_pr__nfet_01v8 L={L} W={W} nf=1 ad='int((nf+1)/2) * W/nf * 0.29' as='int((nf+2)/2) * W/nf * 0.29'
+ pd='2*int((nf+1)/2) * (W/nf + 0.29)' ps='2*int((nf+2)/2) * (W/nf + 0.29)' nrd='0.29 / W' nrs='0.29 / W'
+ sa=0 sb=0 sd=0 mult=1 m=1
XM69 C-drive net34 net35 GND sky130_fd_pr__nfet_01v8 L={L} W={W} nf=1 ad='int((nf+1)/2) * W/nf * 0.29'
+ as='int((nf+2)/2) * W/nf * 0.29' pd='2*int((nf+1)/2) * (W/nf + 0.29)' ps='2*int((nf+2)/2) * (W/nf + 0.29)'
+ nrd='0.29 / W' nrs='0.29 / W' sa=0 sb=0 sd=0 mult=1 m=1
XM113 C-primedrive Db net34 GND sky130_fd_pr__nfet_01v8 L={L} W={W} nf=1 ad='int((nf+1)/2) * W/nf * 0.29'
+ as='int((nf+2)/2) * W/nf * 0.29' pd='2*int((nf+1)/2) * (W/nf + 0.29)' ps='2*int((nf+2)/2) * (W/nf + 0.29)'
+ nrd='0.29 / W' nrs='0.29 / W' sa=0 sb=0 sd=0 mult=1 m=1
XM114 C-primedrive net34 net36 GND sky130_fd_pr__nfet_01v8 L={L} W={W} nf=1 ad='int((nf+1)/2) * W/nf * 0.29'
+ as='int((nf+2)/2) * W/nf * 0.29' pd='2*int((nf+1)/2) * (W/nf + 0.29)' ps='2*int((nf+2)/2) * (W/nf + 0.29)'
+ nrd='0.29 / W' nrs='0.29 / W' sa=0 sb=0 sd=0 mult=1 m=1
XM115 net35 D net37 GND sky130_fd_pr__nfet_01v8 L={L} W={W} nf=1 ad='int((nf+1)/2) * W/nf * 0.29' as='int((nf+2)/2) * W/nf * 0.29'
+ pd='2*int((nf+1)/2) * (W/nf + 0.29)' ps='2*int((nf+2)/2) * (W/nf + 0.29)' nrd='0.29 / W' nrs='0.29 / W'
+ sa=0 sb=0 sd=0 mult=1 m=1
XM116 net35 net37 GND GND sky130_fd_pr__nfet_01v8 L={L} W={W} nf=1 ad='int((nf+1)/2) * W/nf * 0.29' as='int((nf+2)/2) * W/nf * 0.29'
+ pd='2*int((nf+1)/2) * (W/nf + 0.29)' ps='2*int((nf+2)/2) * (W/nf + 0.29)' nrd='0.29 / W' nrs='0.29 / W'
+ sa=0 sb=0 sd=0 mult=1 m=1
XM117 net36 Db net37 GND sky130_fd_pr__nfet_01v8 L={L} W={W} nf=1 ad='int((nf+1)/2) * W/nf * 0.29' as='int((nf+2)/2) * W/nf * 0.29'
+ pd='2*int((nf+1)/2) * (W/nf + 0.29)' ps='2*int((nf+2)/2) * (W/nf + 0.29)' nrd='0.29 / W' nrs='0.29 / W'
+ sa=0 sb=0 sd=0 mult=1 m=1
XM118 net36 net37 GND GND sky130_fd_pr__nfet_01v8 L={L} W={W} nf=1 ad='int((nf+1)/2) * W/nf * 0.29' as='int((nf+2)/2) * W/nf * 0.29'
+ pd='2*int((nf+1)/2) * (W/nf + 0.29)' ps='2*int((nf+2)/2) * (W/nf + 0.29)' nrd='0.29 / W' nrs='0.29 / W'
+ sa=0 sb=0 sd=0 mult=1 m=1
XM28 VDD SEN net24 VDD sky130_fd_pr__pfet_01v8 L={L} W={W} nf=1 ad='int((nf+1)/2) * W/nf * 0.29' as='int((nf+2)/2) * W/nf * 0.29'
+ pd='2*int((nf+1)/2) * (W/nf + 0.29)' ps='2*int((nf+2)/2) * (W/nf + 0.29)' nrd='0.29 / W' nrs='0.29 / W'
+ sa=0 sb=0 sd=0 mult=1 m=1
XM27 STO-b_RCL+b Vcp VDD VDD sky130_fd_pr__pfet_01v8 L={L} W={W} nf=1 ad='int((nf+1)/2) * W/nf * 0.29'
+ as='int((nf+2)/2) * W/nf * 0.29' pd='2*int((nf+1)/2) * (W/nf + 0.29)' ps='2*int((nf+2)/2) * (W/nf + 0.29)'
+ nrd='0.29 / W' nrs='0.29 / W' sa=0 sb=0 sd=0 mult=1 m=1
XM34 STO-_RCL+ net24 VDD VDD sky130_fd_pr__pfet_01v8 L={L} W={W} nf=1 ad='int((nf+1)/2) * W/nf * 0.29'
+ as='int((nf+2)/2) * W/nf * 0.29' pd='2*int((nf+1)/2) * (W/nf + 0.29)' ps='2*int((nf+2)/2) * (W/nf + 0.29)'
+ nrd='0.29 / W' nrs='0.29 / W' sa=0 sb=0 sd=0 mult=1 m=1
XM31 net26 D GND GND sky130_fd_pr__nfet_01v8 L={L} W={W} nf=1 ad='int((nf+1)/2) * W/nf * 0.29' as='int((nf+2)/2) * W/nf * 0.29'
+ pd='2*int((nf+1)/2) * (W/nf + 0.29)' ps='2*int((nf+2)/2) * (W/nf + 0.29)' nrd='0.29 / W' nrs='0.29 / W'
+ sa=0 sb=0 sd=0 mult=1 m=1
XM32 STO-b_RCL+b SEN net25 GND sky130_fd_pr__nfet_01v8 L={L} W={W} nf=1 ad='int((nf+1)/2) * W/nf * 0.29'
+ as='int((nf+2)/2) * W/nf * 0.29' pd='2*int((nf+1)/2) * (W/nf + 0.29)' ps='2*int((nf+2)/2) * (W/nf + 0.29)'
+ nrd='0.29 / W' nrs='0.29 / W' sa=0 sb=0 sd=0 mult=1 m=1
XM33 net25 D GND GND sky130_fd_pr__nfet_01v8 L={L} W={W} nf=1 ad='int((nf+1)/2) * W/nf * 0.29' as='int((nf+2)/2) * W/nf * 0.29'
+ pd='2*int((nf+1)/2) * (W/nf + 0.29)' ps='2*int((nf+2)/2) * (W/nf + 0.29)' nrd='0.29 / W' nrs='0.29 / W'
+ sa=0 sb=0 sd=0 mult=1 m=1
XM35 STO-_RCL+ Vcp GND GND sky130_fd_pr__nfet_01v8 L={L} W={W} nf=1 ad='int((nf+1)/2) * W/nf * 0.29'
+ as='int((nf+2)/2) * W/nf * 0.29' pd='2*int((nf+1)/2) * (W/nf + 0.29)' ps='2*int((nf+2)/2) * (W/nf + 0.29)'
+ nrd='0.29 / W' nrs='0.29 / W' sa=0 sb=0 sd=0 mult=1 m=1
XM45 net30 CompOutb VDD VDD sky130_fd_pr__pfet_01v8 L={L} W={W} nf=1 ad='int((nf+1)/2) * W/nf * 0.29'
+ as='int((nf+2)/2) * W/nf * 0.29' pd='2*int((nf+1)/2) * (W/nf + 0.29)' ps='2*int((nf+2)/2) * (W/nf + 0.29)'
+ nrd='0.29 / W' nrs='0.29 / W' sa=0 sb=0 sd=0 mult=1 m=1
XM46 net30 ENADb D VDD sky130_fd_pr__pfet_01v8 L={L} W={W} nf=1 ad='int((nf+1)/2) * W/nf * 0.29' as='int((nf+2)/2) * W/nf * 0.29'
+ pd='2*int((nf+1)/2) * (W/nf + 0.29)' ps='2*int((nf+2)/2) * (W/nf + 0.29)' nrd='0.29 / W' nrs='0.29 / W'
+ sa=0 sb=0 sd=0 mult=1 m=1
XM47 VDD CompOut net31 VDD sky130_fd_pr__pfet_01v8 L={L} W={W} nf=1 ad='int((nf+1)/2) * W/nf * 0.29'
+ as='int((nf+2)/2) * W/nf * 0.29' pd='2*int((nf+1)/2) * (W/nf + 0.29)' ps='2*int((nf+2)/2) * (W/nf + 0.29)'
+ nrd='0.29 / W' nrs='0.29 / W' sa=0 sb=0 sd=0 mult=1 m=1
XM48 Db ENADb net31 VDD sky130_fd_pr__pfet_01v8 L={L} W={W} nf=1 ad='int((nf+1)/2) * W/nf * 0.29' as='int((nf+2)/2) * W/nf * 0.29'
+ pd='2*int((nf+1)/2) * (W/nf + 0.29)' ps='2*int((nf+2)/2) * (W/nf + 0.29)' nrd='0.29 / W' nrs='0.29 / W'
+ sa=0 sb=0 sd=0 mult=1 m=1
XM49 net33 ENAD D GND sky130_fd_pr__nfet_01v8 L={L} W={W} nf=1 ad='int((nf+1)/2) * W/nf * 0.29' as='int((nf+2)/2) * W/nf * 0.29'
+ pd='2*int((nf+1)/2) * (W/nf + 0.29)' ps='2*int((nf+2)/2) * (W/nf + 0.29)' nrd='0.29 / W' nrs='0.29 / W'
+ sa=0 sb=0 sd=0 mult=1 m=1
XM68 net33 CompOutb GND GND sky130_fd_pr__nfet_01v8 L={L} W={W} nf=1 ad='int((nf+1)/2) * W/nf * 0.29'
+ as='int((nf+2)/2) * W/nf * 0.29' pd='2*int((nf+1)/2) * (W/nf + 0.29)' ps='2*int((nf+2)/2) * (W/nf + 0.29)'
+ nrd='0.29 / W' nrs='0.29 / W' sa=0 sb=0 sd=0 mult=1 m=1
XM70 Db ENAD net32 GND sky130_fd_pr__nfet_01v8 L={L} W={W} nf=1 ad='int((nf+1)/2) * W/nf * 0.29' as='int((nf+2)/2) * W/nf * 0.29'
+ pd='2*int((nf+1)/2) * (W/nf + 0.29)' ps='2*int((nf+2)/2) * (W/nf + 0.29)' nrd='0.29 / W' nrs='0.29 / W'
+ sa=0 sb=0 sd=0 mult=1 m=1
XM71 GND CompOut net32 GND sky130_fd_pr__nfet_01v8 L={L} W={W} nf=1 ad='int((nf+1)/2) * W/nf * 0.29'
+ as='int((nf+2)/2) * W/nf * 0.29' pd='2*int((nf+1)/2) * (W/nf + 0.29)' ps='2*int((nf+2)/2) * (W/nf + 0.29)'
+ nrd='0.29 / W' nrs='0.29 / W' sa=0 sb=0 sd=0 mult=1 m=1
XM36 net27 Db VDD VDD sky130_fd_pr__pfet_01v8 L={L} W={W} nf=1 ad='int((nf+1)/2) * W/nf * 0.29' as='int((nf+2)/2) * W/nf * 0.29'
+ pd='2*int((nf+1)/2) * (W/nf + 0.29)' ps='2*int((nf+2)/2) * (W/nf + 0.29)' nrd='0.29 / W' nrs='0.29 / W'
+ sa=0 sb=0 sd=0 mult=1 m=1
XM37 VDD SEN net27 VDD sky130_fd_pr__pfet_01v8 L={L} W={W} nf=1 ad='int((nf+1)/2) * W/nf * 0.29' as='int((nf+2)/2) * W/nf * 0.29'
+ pd='2*int((nf+1)/2) * (W/nf + 0.29)' ps='2*int((nf+2)/2) * (W/nf + 0.29)' nrd='0.29 / W' nrs='0.29 / W'
+ sa=0 sb=0 sd=0 mult=1 m=1
XM38 STO+b_RCL-b Vcp VDD VDD sky130_fd_pr__pfet_01v8 L={L} W={W} nf=1 ad='int((nf+1)/2) * W/nf * 0.29'
+ as='int((nf+2)/2) * W/nf * 0.29' pd='2*int((nf+1)/2) * (W/nf + 0.29)' ps='2*int((nf+2)/2) * (W/nf + 0.29)'
+ nrd='0.29 / W' nrs='0.29 / W' sa=0 sb=0 sd=0 mult=1 m=1
XM43 STO+_RCL- net27 VDD VDD sky130_fd_pr__pfet_01v8 L={L} W={W} nf=1 ad='int((nf+1)/2) * W/nf * 0.29'
+ as='int((nf+2)/2) * W/nf * 0.29' pd='2*int((nf+1)/2) * (W/nf + 0.29)' ps='2*int((nf+2)/2) * (W/nf + 0.29)'
+ nrd='0.29 / W' nrs='0.29 / W' sa=0 sb=0 sd=0 mult=1 m=1
XM39 net27 SEN net29 GND sky130_fd_pr__nfet_01v8 L={L} W={W} nf=1 ad='int((nf+1)/2) * W/nf * 0.29' as='int((nf+2)/2) * W/nf * 0.29'
+ pd='2*int((nf+1)/2) * (W/nf + 0.29)' ps='2*int((nf+2)/2) * (W/nf + 0.29)' nrd='0.29 / W' nrs='0.29 / W'
+ sa=0 sb=0 sd=0 mult=1 m=1
XM40 STO+b_RCL-b SEN net28 GND sky130_fd_pr__nfet_01v8 L={L} W={W} nf=1 ad='int((nf+1)/2) * W/nf * 0.29'
+ as='int((nf+2)/2) * W/nf * 0.29' pd='2*int((nf+1)/2) * (W/nf + 0.29)' ps='2*int((nf+2)/2) * (W/nf + 0.29)'
+ nrd='0.29 / W' nrs='0.29 / W' sa=0 sb=0 sd=0 mult=1 m=1
XM41 net29 Db GND GND sky130_fd_pr__nfet_01v8 L={L} W={W} nf=1 ad='int((nf+1)/2) * W/nf * 0.29' as='int((nf+2)/2) * W/nf * 0.29'
+ pd='2*int((nf+1)/2) * (W/nf + 0.29)' ps='2*int((nf+2)/2) * (W/nf + 0.29)' nrd='0.29 / W' nrs='0.29 / W'
+ sa=0 sb=0 sd=0 mult=1 m=1
XM42 net28 Db GND GND sky130_fd_pr__nfet_01v8 L={L} W={W} nf=1 ad='int((nf+1)/2) * W/nf * 0.29' as='int((nf+2)/2) * W/nf * 0.29'
+ pd='2*int((nf+1)/2) * (W/nf + 0.29)' ps='2*int((nf+2)/2) * (W/nf + 0.29)' nrd='0.29 / W' nrs='0.29 / W'
+ sa=0 sb=0 sd=0 mult=1 m=1
XM44 STO+_RCL- Vcp GND GND sky130_fd_pr__nfet_01v8 L={L} W={W} nf=1 ad='int((nf+1)/2) * W/nf * 0.29'
+ as='int((nf+2)/2) * W/nf * 0.29' pd='2*int((nf+1)/2) * (W/nf + 0.29)' ps='2*int((nf+2)/2) * (W/nf + 0.29)'
+ nrd='0.29 / W' nrs='0.29 / W' sa=0 sb=0 sd=0 mult=1 m=1
XM126 net40 Vb net38 GND sky130_fd_pr__nfet_01v8 L=0.5 W=12 nf=1 ad='int((nf+1)/2) * W/nf * 0.29' as='int((nf+2)/2) * W/nf * 0.29'
+ pd='2*int((nf+1)/2) * (W/nf + 0.29)' ps='2*int((nf+2)/2) * (W/nf + 0.29)' nrd='0.29 / W' nrs='0.29 / W'
+ sa=0 sb=0 sd=0 mult=8 m=8
XM127 Vb Vb GND GND sky130_fd_pr__nfet_01v8 L=0.5 W=12 nf=1 ad='int((nf+1)/2) * W/nf * 0.29' as='int((nf+2)/2) * W/nf * 0.29'
+ pd='2*int((nf+1)/2) * (W/nf + 0.29)' ps='2*int((nf+2)/2) * (W/nf + 0.29)' nrd='0.29 / W' nrs='0.29 / W'
+ sa=0 sb=0 sd=0 mult=1 m=1
XM128 VDD net38 net38 VDD sky130_fd_pr__pfet_01v8 L=0.5 W=12 nf=1 ad='int((nf+1)/2) * W/nf * 0.29' as='int((nf+2)/2) * W/nf * 0.29'
+ pd='2*int((nf+1)/2) * (W/nf + 0.29)' ps='2*int((nf+2)/2) * (W/nf + 0.29)' nrd='0.29 / W' nrs='0.29 / W'
+ sa=0 sb=0 sd=0 mult=1 m=1
XM129 Vb net38 VDD VDD sky130_fd_pr__pfet_01v8 L=0.5 W=12 nf=1 ad='int((nf+1)/2) * W/nf * 0.29' as='int((nf+2)/2) * W/nf * 0.29'
+ pd='2*int((nf+1)/2) * (W/nf + 0.29)' ps='2*int((nf+2)/2) * (W/nf + 0.29)' nrd='0.29 / W' nrs='0.29 / W'
+ sa=0 sb=0 sd=0 mult=1 m=1
R2 net40 GND 2.2k m=1
XM21 net41 Vcp net39 GND sky130_fd_pr__nfet_01v8 L=0.5 W=12 nf=1 ad='int((nf+1)/2) * W/nf * 0.29' as='int((nf+2)/2) * W/nf * 0.29'
+ pd='2*int((nf+1)/2) * (W/nf + 0.29)' ps='2*int((nf+2)/2) * (W/nf + 0.29)' nrd='0.29 / W' nrs='0.29 / W'
+ sa=0 sb=0 sd=0 mult=8 m=8
XM22 Vcp Vcp GND GND sky130_fd_pr__nfet_01v8 L=0.5 W=12 nf=1 ad='int((nf+1)/2) * W/nf * 0.29' as='int((nf+2)/2) * W/nf * 0.29'
+ pd='2*int((nf+1)/2) * (W/nf + 0.29)' ps='2*int((nf+2)/2) * (W/nf + 0.29)' nrd='0.29 / W' nrs='0.29 / W'
+ sa=0 sb=0 sd=0 mult=1 m=1
XM23 VDD net39 net39 VDD sky130_fd_pr__pfet_01v8 L=0.5 W=12 nf=1 ad='int((nf+1)/2) * W/nf * 0.29' as='int((nf+2)/2) * W/nf * 0.29'
+ pd='2*int((nf+1)/2) * (W/nf + 0.29)' ps='2*int((nf+2)/2) * (W/nf + 0.29)' nrd='0.29 / W' nrs='0.29 / W'
+ sa=0 sb=0 sd=0 mult=1 m=1
XM24 Vcp net39 VDD VDD sky130_fd_pr__pfet_01v8 L=0.5 W=12 nf=1 ad='int((nf+1)/2) * W/nf * 0.29' as='int((nf+2)/2) * W/nf * 0.29'
+ pd='2*int((nf+1)/2) * (W/nf + 0.29)' ps='2*int((nf+2)/2) * (W/nf + 0.29)' nrd='0.29 / W' nrs='0.29 / W'
+ sa=0 sb=0 sd=0 mult=1 m=1
R1 net41 GND 800 m=1
**.ends
.GLOBAL GND
.GLOBAL VDD
.end
